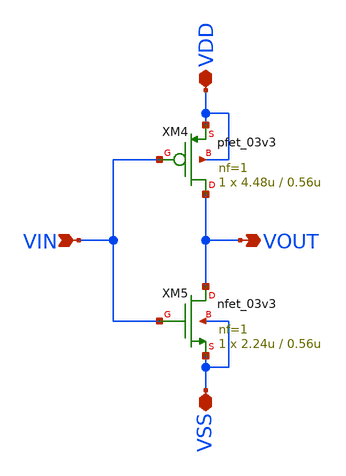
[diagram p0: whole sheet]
** sch_path: PLL-main/schematic/xschem/inverter_1.sch
* Copyright 2022 GlobalFoundries PDK Authors
* Licensed under the Apache License, Version 2.0 (the "License");
* you may not use this file except in compliance with the License.
* You may obtain a copy of the License at
* https://www.apache.org/licenses/LICENSE-2.0
* Unless required by applicable law or agreed to in writing, software
* distributed under the License is distributed on an "AS IS" BASIS,
* WITHOUT WARRANTIES OR CONDITIONS OF ANY KIND, either express or implied.
* See the License for the specific language governing permissions and
* limitations under the License.
**.subckt inverter_1 VDD VIN VOUT VSS
*.iopin VDD
*.ipin VIN
*.opin VOUT
*.iopin VSS
XM4 VOUT VIN VDD VDD pfet_03v3 L=0.56u W=4.48u nf=1 ad='int((nf+1)/2) * W/nf * 0.18u' as='int((nf+2)/2) * W/nf * 0.18u'
+ pd='2*int((nf+1)/2) * (W/nf + 0.18u)' ps='2*int((nf+2)/2) * (W/nf + 0.18u)' nrd='0.18u / W' nrs='0.18u / W'
+ sa=0 sb=0 sd=0 m=1
XM5 VOUT VIN VSS VSS nfet_03v3 L=0.56u W=2.24u nf=1 ad='int((nf+1)/2) * W/nf * 0.18u' as='int((nf+2)/2) * W/nf * 0.18u'
+ pd='2*int((nf+1)/2) * (W/nf + 0.18u)' ps='2*int((nf+2)/2) * (W/nf + 0.18u)' nrd='0.18u / W' nrs='0.18u / W'
+ sa=0 sb=0 sd=0 m=1
**.ends
.end
